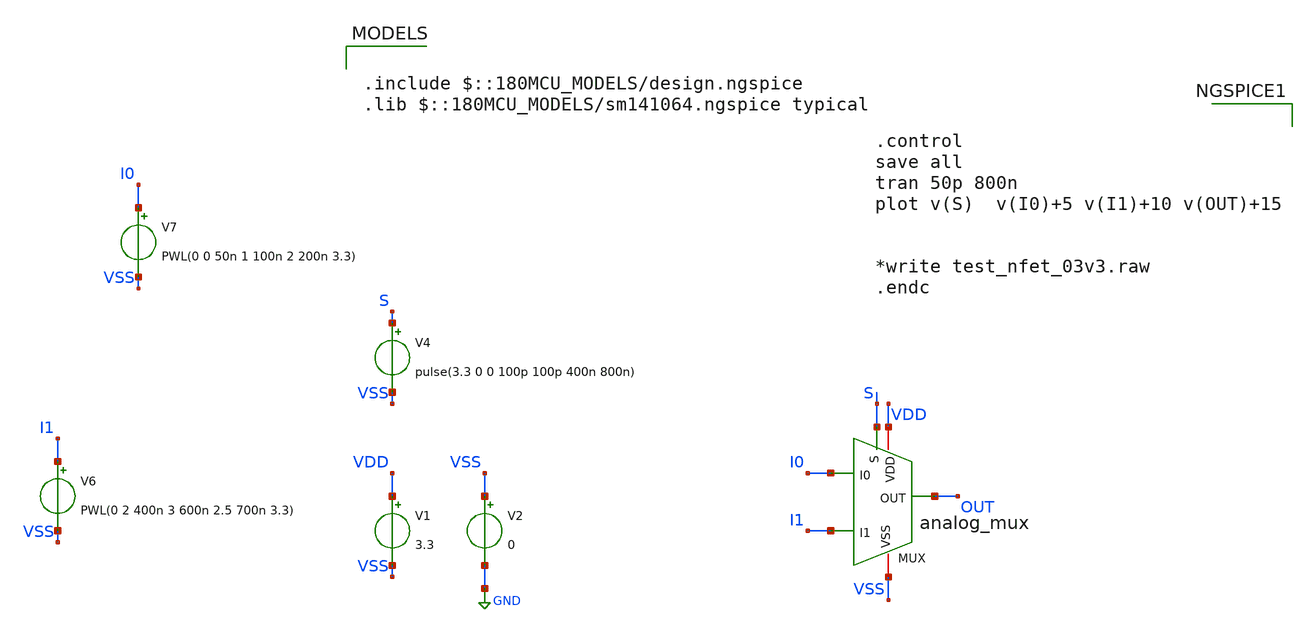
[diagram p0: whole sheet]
** sch_path: Clock_Generator_PAKISTAN_02/Schematics/analog_mux_test.sch
**.subckt analog_mux_test
x1 S VSS VDD OUT I1 I0 analog_mux
V1 VDD VSS 3.3
V2 VSS GND 0
V4 S VSS pulse(3.3 0 0 100p 100p 400n 800n)
V6 I1 VSS PWL(0 2 400n 3 600n 2.5 700n 3.3)
V7 I0 VSS PWL(0 0 50n 1 100n 2 200n 3.3)
**** begin user architecture code


.control
save all
tran 50p 800n
plot v(S)  v(I0)+5 v(I1)+10 v(OUT)+15


*write test_nfet_03v3.raw
.endc



.include $::180MCU_MODELS/design.ngspice
.lib $::180MCU_MODELS/sm141064.ngspice typical

**** end user architecture code
**.ends
.GLOBAL GND
.end
